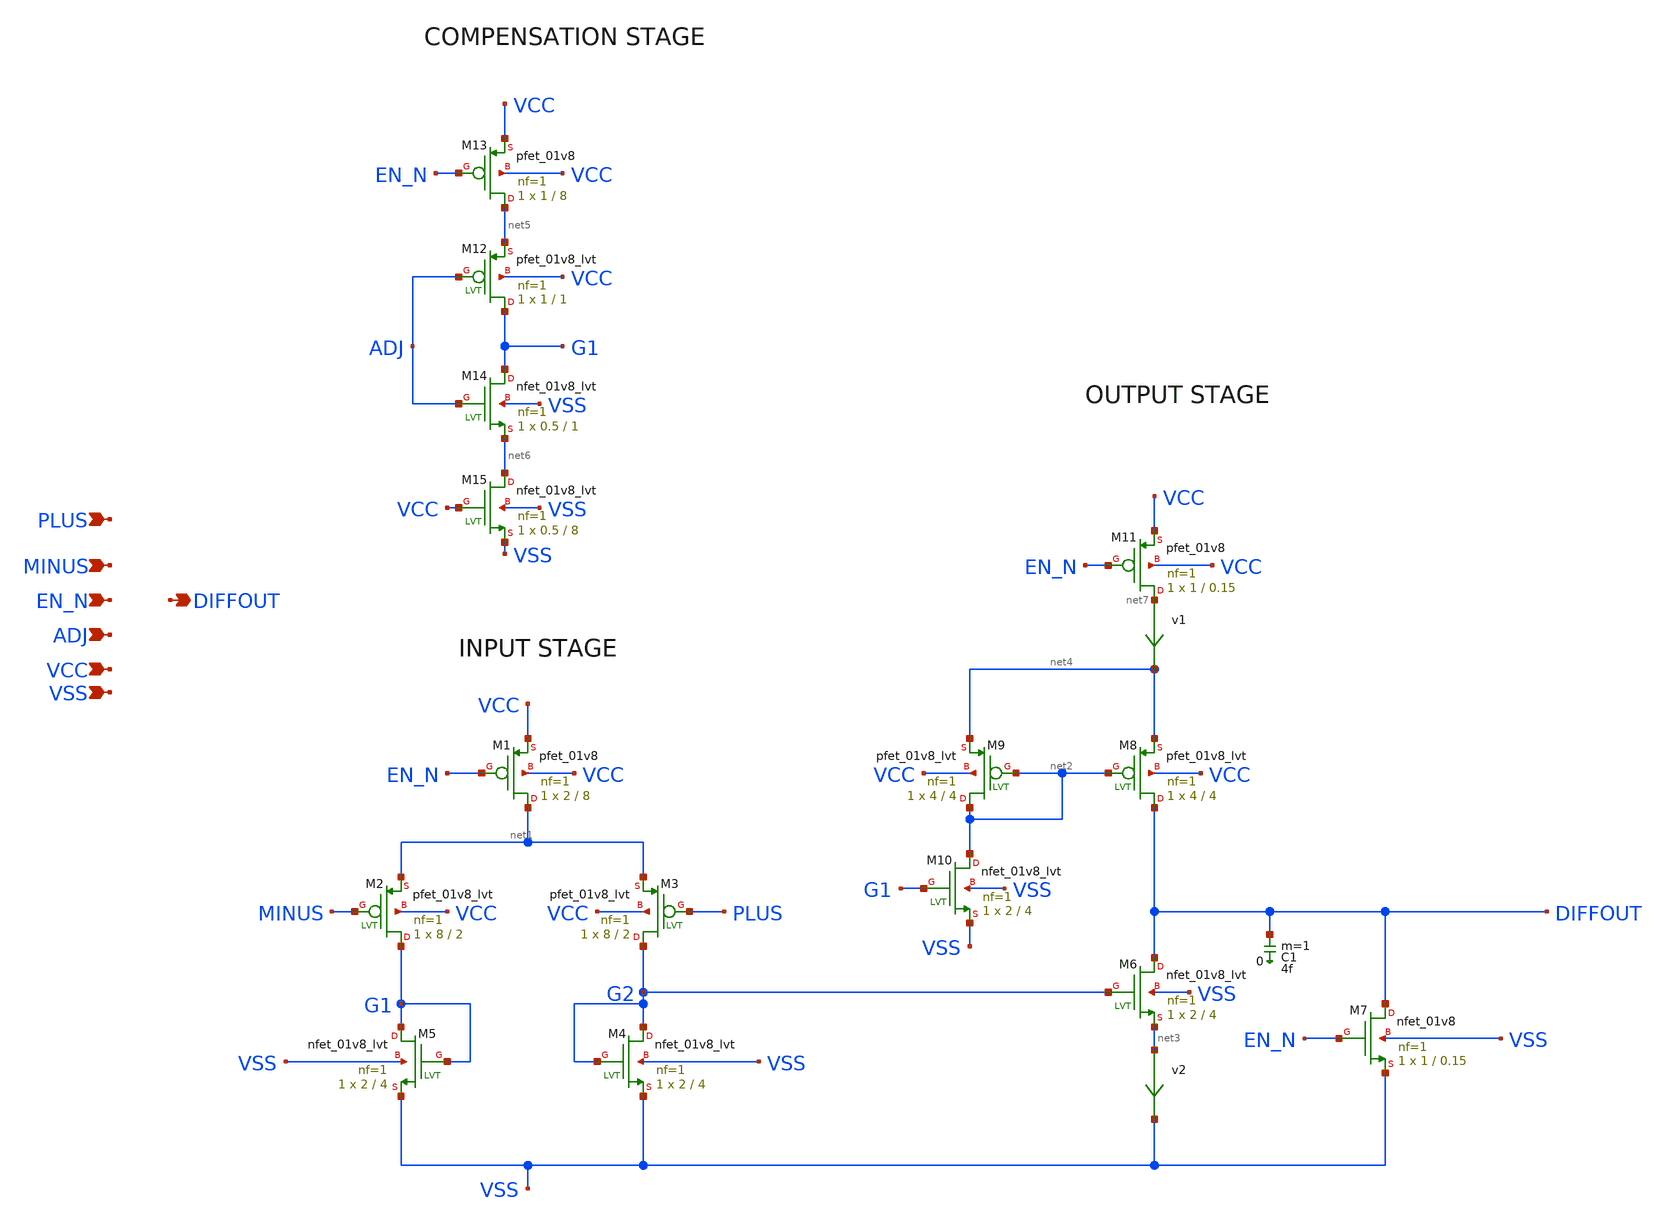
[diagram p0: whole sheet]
** sch_path: analog/comparator-sky130/opam.sch
**.subckt opam PLUS MINUS EN_N VCC VSS ADJ DIFFOUT
*.ipin PLUS
*.ipin MINUS
*.ipin EN_N
*.ipin VCC
*.ipin VSS
*.ipin ADJ
*.opin DIFFOUT
XM1 net1 EN_N VCC VCC sky130_fd_pr__pfet_01v8 L=8 W=2 nf=1 ad='int((1 + 1)/2) * 2 / 1 * 0.29' as='int((1 + 2)/2) * 2 / 1 * 0.29'
+ pd='2*int((1 + 1)/2) * (2 / 1 + 0.29)' ps='2*int((1 + 2)/2) * (2 / 1 + 0.29)' nrd='0.29 / 2 ' nrs='0.29 / 2 '
+ sa=0 sb=0 sd=0 mult=1 m=1
XM2 G1 MINUS net1 VCC sky130_fd_pr__pfet_01v8_lvt L=2 W=8 nf=1 ad='int((1 + 1)/2) * 8 / 1 * 0.29' as='int((1 + 2)/2) * 8 / 1 * 0.29'
+ pd='2*int((1 + 1)/2) * (8 / 1 + 0.29)' ps='2*int((1 + 2)/2) * (8 / 1 + 0.29)' nrd='0.29 / 8 ' nrs='0.29 / 8 '
+ sa=0 sb=0 sd=0 mult=1 m=1
XM3 G2 PLUS net1 VCC sky130_fd_pr__pfet_01v8_lvt L=2 W=8 nf=1 ad='int((1 + 1)/2) * 8 / 1 * 0.29' as='int((1 + 2)/2) * 8 / 1 * 0.29'
+ pd='2*int((1 + 1)/2) * (8 / 1 + 0.29)' ps='2*int((1 + 2)/2) * (8 / 1 + 0.29)' nrd='0.29 / 8 ' nrs='0.29 / 8 '
+ sa=0 sb=0 sd=0 mult=1 m=1
XM4 G2 G2 VSS VSS sky130_fd_pr__nfet_01v8_lvt L=4 W=2 nf=1 ad='int((1 + 1)/2) * 2 / 1 * 0.29' as='int((1 + 2)/2) * 2 / 1 * 0.29'
+ pd='2*int((1 + 1)/2) * (2 / 1 + 0.29)' ps='2*int((1 + 2)/2) * (2 / 1 + 0.29)' nrd='0.29 / 2 ' nrs='0.29 / 2 '
+ sa=0 sb=0 sd=0 mult=1 m=1
XM5 G1 G1 VSS VSS sky130_fd_pr__nfet_01v8_lvt L=4 W=2 nf=1 ad='int((1 + 1)/2) * 2 / 1 * 0.29' as='int((1 + 2)/2) * 2 / 1 * 0.29'
+ pd='2*int((1 + 1)/2) * (2 / 1 + 0.29)' ps='2*int((1 + 2)/2) * (2 / 1 + 0.29)' nrd='0.29 / 2 ' nrs='0.29 / 2 '
+ sa=0 sb=0 sd=0 mult=1 m=1
XM6 DIFFOUT G2 net3 VSS sky130_fd_pr__nfet_01v8_lvt L=4 W=2 nf=1 ad='int((1 + 1)/2) * 2 / 1 * 0.29' as='int((1 + 2)/2) * 2 / 1 * 0.29'
+ pd='2*int((1 + 1)/2) * (2 / 1 + 0.29)' ps='2*int((1 + 2)/2) * (2 / 1 + 0.29)' nrd='0.29 / 2 ' nrs='0.29 / 2 '
+ sa=0 sb=0 sd=0 mult=1 m=1
XM7 DIFFOUT EN_N VSS VSS sky130_fd_pr__nfet_01v8 L=0.15 W=1 nf=1 ad='int((1 + 1)/2) * 1 / 1 * 0.29' as='int((1 + 2)/2) * 1 / 1 * 0.29'
+ pd='2*int((1 + 1)/2) * (1 / 1 + 0.29)' ps='2*int((1 + 2)/2) * (1 / 1 + 0.29)' nrd='0.29 / 1 ' nrs='0.29 / 1 '
+ sa=0 sb=0 sd=0 mult=1 m=1
XM8 DIFFOUT net2 net4 VCC sky130_fd_pr__pfet_01v8_lvt L=4 W=4 nf=1 ad='int((1 + 1)/2) * 4 / 1 * 0.29'
+ as='int((1 + 2)/2) * 4 / 1 * 0.29' pd='2*int((1 + 1)/2) * (4 / 1 + 0.29)' ps='2*int((1 + 2)/2) * (4 / 1 + 0.29)'
+ nrd='0.29 / 4 ' nrs='0.29 / 4 ' sa=0 sb=0 sd=0 mult=1 m=1
XM9 net2 net2 net4 VCC sky130_fd_pr__pfet_01v8_lvt L=4 W=4 nf=1 ad='int((1 + 1)/2) * 4 / 1 * 0.29' as='int((1 + 2)/2) * 4 / 1 * 0.29'
+ pd='2*int((1 + 1)/2) * (4 / 1 + 0.29)' ps='2*int((1 + 2)/2) * (4 / 1 + 0.29)' nrd='0.29 / 4 ' nrs='0.29 / 4 '
+ sa=0 sb=0 sd=0 mult=1 m=1
XM10 net2 G1 VSS VSS sky130_fd_pr__nfet_01v8_lvt L=4 W=2 nf=1 ad='int((1 + 1)/2) * 2 / 1 * 0.29' as='int((1 + 2)/2) * 2 / 1 * 0.29'
+ pd='2*int((1 + 1)/2) * (2 / 1 + 0.29)' ps='2*int((1 + 2)/2) * (2 / 1 + 0.29)' nrd='0.29 / 2 ' nrs='0.29 / 2 '
+ sa=0 sb=0 sd=0 mult=1 m=1
XM11 net7 EN_N VCC VCC sky130_fd_pr__pfet_01v8 L=0.15 W=1 nf=1 ad='int((1 + 1)/2) * 1 / 1 * 0.29' as='int((1 + 2)/2) * 1 / 1 * 0.29'
+ pd='2*int((1 + 1)/2) * (1 / 1 + 0.29)' ps='2*int((1 + 2)/2) * (1 / 1 + 0.29)' nrd='0.29 / 1 ' nrs='0.29 / 1 '
+ sa=0 sb=0 sd=0 mult=1 m=1
C1 DIFFOUT 0 4f m=1
v2 net3 VSS 0
.save i(v2)
v1 net7 net4 0
.save i(v1)
XM12 G1 ADJ net5 VCC sky130_fd_pr__pfet_01v8_lvt L=1 W=1 nf=1 ad='int((1 + 1)/2) * 1 / 1 * 0.29' as='int((1 + 2)/2) * 1 / 1 * 0.29'
+ pd='2*int((1 + 1)/2) * (1 / 1 + 0.29)' ps='2*int((1 + 2)/2) * (1 / 1 + 0.29)' nrd='0.29 / 1 ' nrs='0.29 / 1 '
+ sa=0 sb=0 sd=0 mult=1 m=1
XM13 net5 EN_N VCC VCC sky130_fd_pr__pfet_01v8 L=8 W=1 nf=1 ad='int((1 + 1)/2) * 1 / 1 * 0.29' as='int((1 + 2)/2) * 1 / 1 * 0.29'
+ pd='2*int((1 + 1)/2) * (1 / 1 + 0.29)' ps='2*int((1 + 2)/2) * (1 / 1 + 0.29)' nrd='0.29 / 1 ' nrs='0.29 / 1 '
+ sa=0 sb=0 sd=0 mult=1 m=1
XM14 G1 ADJ net6 VSS sky130_fd_pr__nfet_01v8_lvt L=1 W=0.5 nf=1 ad='int((1 + 1)/2) * 0.5 / 1 * 0.29'
+ as='int((1 + 2)/2) * 0.5 / 1 * 0.29' pd='2*int((1 + 1)/2) * (0.5 / 1 + 0.29)' ps='2*int((1 + 2)/2) * (0.5 / 1 + 0.29)'
+ nrd='0.29 / 0.5 ' nrs='0.29 / 0.5 ' sa=0 sb=0 sd=0 mult=1 m=1
XM15 net6 VCC VSS VSS sky130_fd_pr__nfet_01v8_lvt L=8 W=0.5 nf=1 ad='int((1 + 1)/2) * 0.5 / 1 * 0.29'
+ as='int((1 + 2)/2) * 0.5 / 1 * 0.29' pd='2*int((1 + 1)/2) * (0.5 / 1 + 0.29)' ps='2*int((1 + 2)/2) * (0.5 / 1 + 0.29)'
+ nrd='0.29 / 0.5 ' nrs='0.29 / 0.5 ' sa=0 sb=0 sd=0 mult=1 m=1
**.ends
.end
